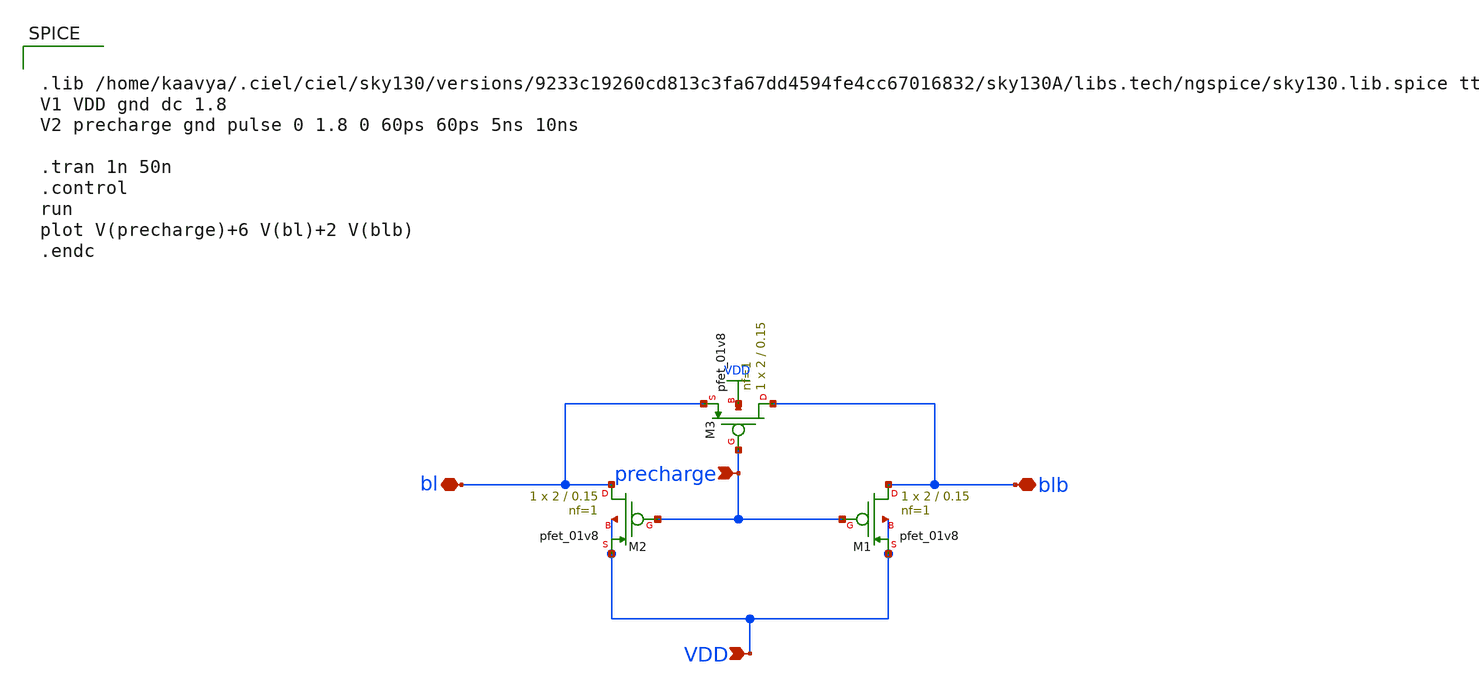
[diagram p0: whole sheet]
** sch_path: xschem/Subcircuits/precharge.sch
**.subckt precharge precharge bl blb VDD
*.ipin precharge
*.iopin bl
*.iopin blb
*.ipin VDD
XM1 blb precharge VDD VDD sky130_fd_pr__pfet_01v8 L=0.15 W=2 nf=1 ad='int((1 + 1)/2) * 2 / 1 * 0.29'
+ as='int((1 + 2)/2) * 2 / 1 * 0.29' pd='2*int((1 + 1)/2) * (2 / 1 + 0.29)' ps='2*int((1 + 2)/2) * (2 / 1 + 0.29)'
+ nrd='0.29 / 2 ' nrs='0.29 / 2 ' sa=0 sb=0 sd=0 mult=1 m=1
XM2 bl precharge VDD VDD sky130_fd_pr__pfet_01v8 L=0.15 W=2 nf=1 ad='int((1 + 1)/2) * 2 / 1 * 0.29' as='int((1 + 2)/2) * 2 / 1 * 0.29'
+ pd='2*int((1 + 1)/2) * (2 / 1 + 0.29)' ps='2*int((1 + 2)/2) * (2 / 1 + 0.29)' nrd='0.29 / 2 ' nrs='0.29 / 2 '
+ sa=0 sb=0 sd=0 mult=1 m=1
XM3 blb precharge bl VDD sky130_fd_pr__pfet_01v8 L=0.15 W=2 nf=1 ad='int((1 + 1)/2) * 2 / 1 * 0.29' as='int((1 + 2)/2) * 2 / 1 * 0.29'
+ pd='2*int((1 + 1)/2) * (2 / 1 + 0.29)' ps='2*int((1 + 2)/2) * (2 / 1 + 0.29)' nrd='0.29 / 2 ' nrs='0.29 / 2 '
+ sa=0 sb=0 sd=0 mult=1 m=1
**** begin user architecture code


.lib /home/kaavya/.ciel/ciel/sky130/versions/9233c19260cd813c3fa67dd4594fe4cc67016832/sky130A/libs.tech/ngspice/sky130.lib.spice tt
V1 VDD gnd dc 1.8
V2 precharge gnd pulse 0 1.8 0 60ps 60ps 5ns 10ns

.tran 1n 50n
.control
run
plot V(precharge)+6 V(bl)+2 V(blb)
.endc

**** end user architecture code
**.ends
.GLOBAL VDD
.end
